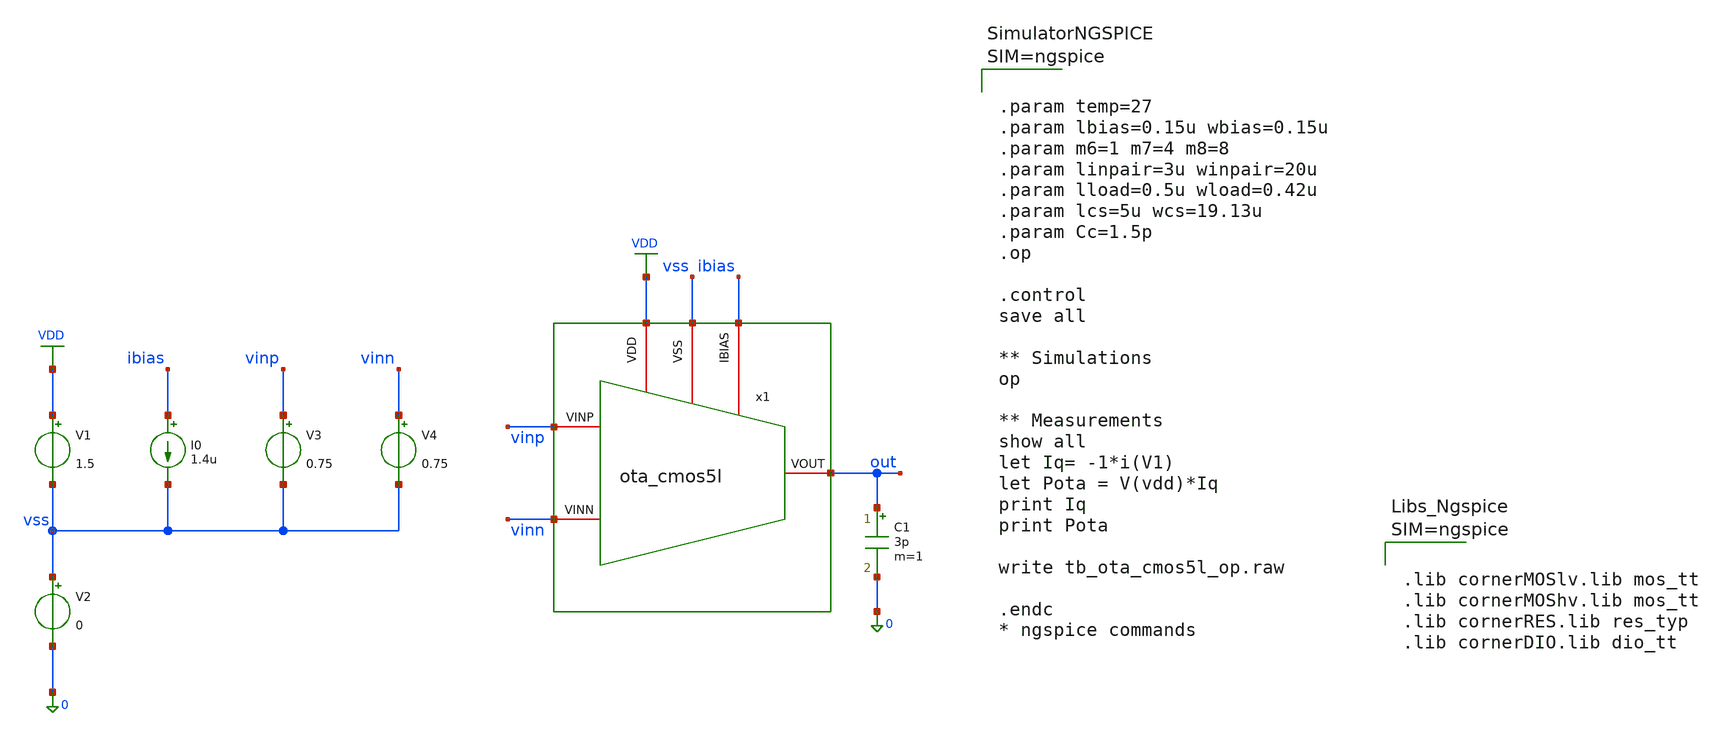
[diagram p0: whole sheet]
** sch_path: designs/libs/tb_analog/tb_ota_cmos5l_op/tb_ota_cmos5l_op.sch
**.subckt tb_ota_cmos5l_op
x1 vss ibias VDD vinn vinp out ota_cmos5l
C1 out 0 3p m=1
I0 ibias vss 1.4u
V1 VDD vss 1.5
V2 vss 0 0
V3 vinp vss 0.75
V4 vinn vss 0.75
**** begin user architecture code



.param temp=27
.param lbias=0.15u wbias=0.15u
.param m6=1 m7=4 m8=8
.param linpair=3u winpair=20u
.param lload=0.5u wload=0.42u
.param lcs=5u wcs=19.13u
.param Cc=1.5p
.op

.control
save all

** Simulations
op

** Measurements
show all
let Iq= -1*i(V1)
let Pota = V(vdd)*Iq
print Iq
print Pota

write tb_ota_cmos5l_op.raw

.endc
* ngspice commands






.lib cornerMOSlv.lib mos_tt
.lib cornerMOShv.lib mos_tt
.lib cornerRES.lib res_typ
.lib cornerDIO.lib dio_tt



**** end user architecture code
**.ends
.GLOBAL VDD
.end
